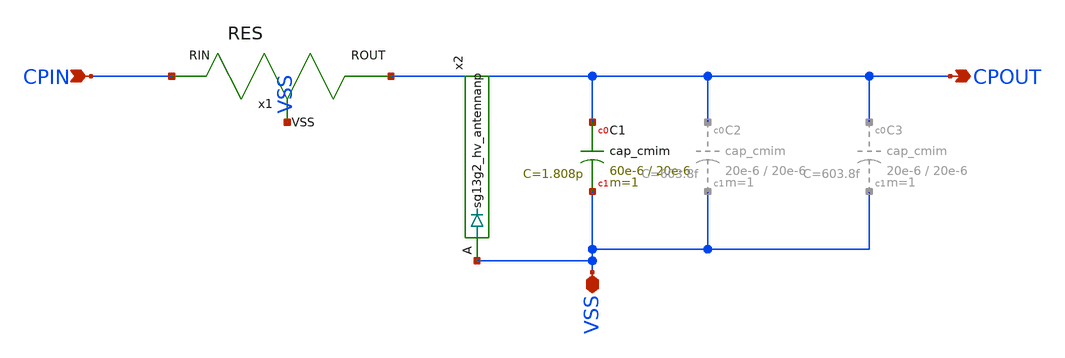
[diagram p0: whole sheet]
** sch_path: QDLL6501-main/schematic/xschem/CP.sch
**.subckt CP VSS CPIN CPOUT
*.iopin VSS
*.ipin CPIN
*.opin CPOUT
XC1 CPOUT VSS cap_cmim w=60e-6 l=20e-6 m=1 mm_ok=1
x1 CPOUT CPIN VSS RES
x2 VSS CPOUT VSS sg13g2_hv_antennanp
**.ends
.end
